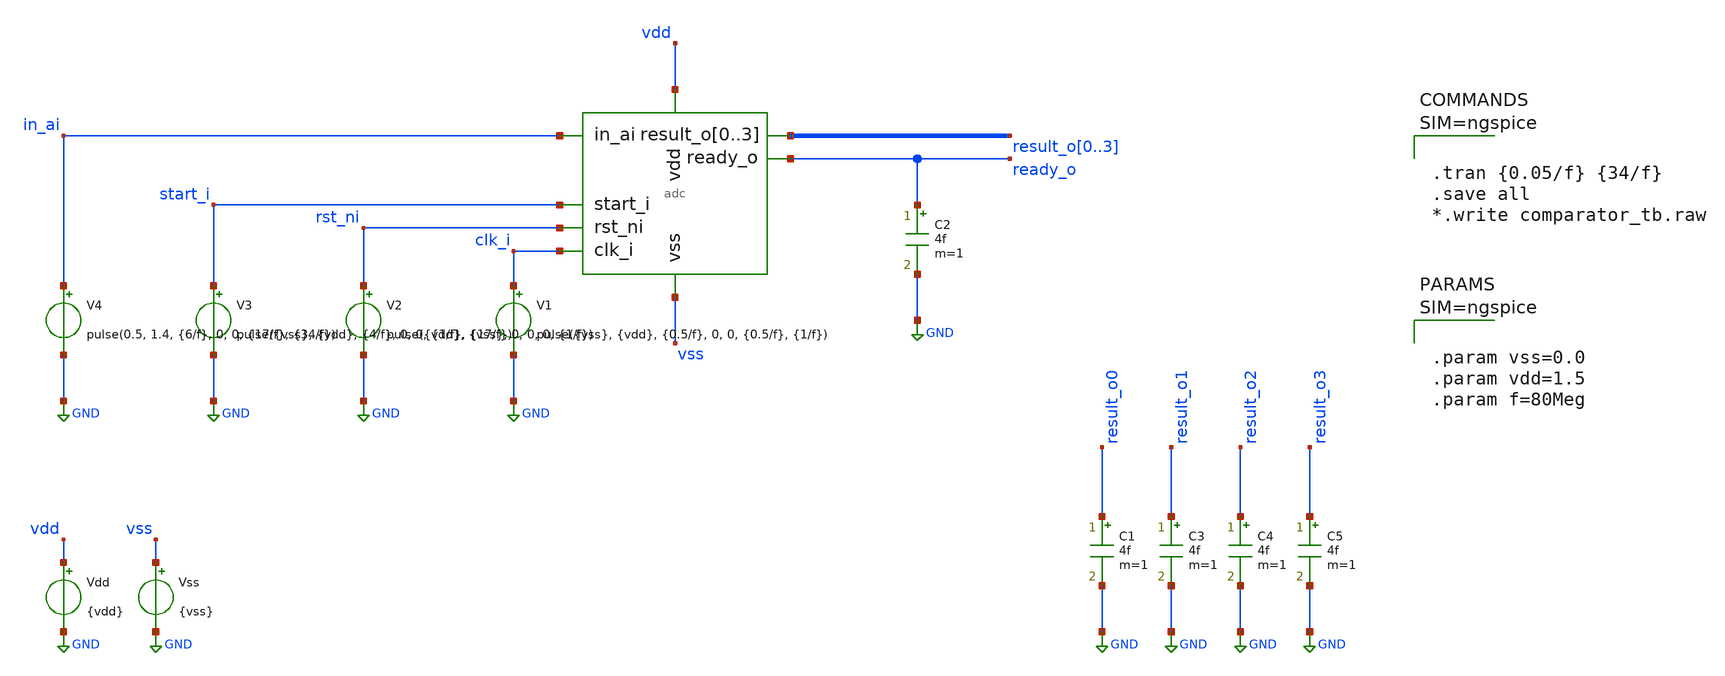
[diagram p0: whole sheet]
** sch_path: designs/basic/adc_tb.sch
**.subckt adc_tb
x1 in_ai start_i rst_ni clk_i result_o0 result_o1 result_o2 result_o3 ready_o vdd vss adc
V1 clk_i GND pulse({vss}, {vdd}, {0.5/f}, 0, 0, {0.5/f}, {1/f})
V2 rst_ni GND pulse({vdd}, {vss}, 0, 0, 0, {1/f})
V3 start_i GND pulse({vss}, {vdd}, {4/f}, 0, 0, {1/f}, {17/f})
V4 in_ai GND pulse(0.5, 1.4, {6/f}, 0, 0, {17/f}, {34/f})
.save i(v4)
Vdd vdd GND {vdd}
Vss vss GND {vss}
C1 result_o0 GND 4f m=1
C2 ready_o GND 4f m=1
C3 result_o1 GND 4f m=1
C4 result_o2 GND 4f m=1
C5 result_o3 GND 4f m=1
**** begin user architecture code

.lib $::SG13G2_MODELS/cornerMOSlv.lib mos_tt
.lib $::SG13G2_MODELS/cornerCAP.lib cap_typ
.include $::PDK_ROOT/ihp-sg13g2/libs.ref/sg13g2_stdcell/spice/sg13g2_stdcell.spice




.tran {0.05/f} {34/f}
.save all
*.write comparator_tb.raw






.param vss=0.0
.param vdd=1.5
.param f=80Meg






.model adc_buff_clk adc_bridge(in_low = 'vdd/2' in_high = 'vdd/2')

.control
pre_set auto_bridge_d_out =  ( ".model auto_bridge_out bidi_bridge(direction=0 out_high=1.5
+ t_rise=1n t_fall=1n)"    "auto_bridge_out%d [ %s ] [ %s ] null auto_bridge_out" )
pre_set auto_bridge_d_in =  ( ".model auto_bridge_in bidi_bridge(direction=1 in_low=0.5 in_high=1)"
+    "auto_bridge_in%d [ %s ] [ %s ] null auto_bridge_in" )
.endc



**** end user architecture code
**.ends
.GLOBAL GND
.end
